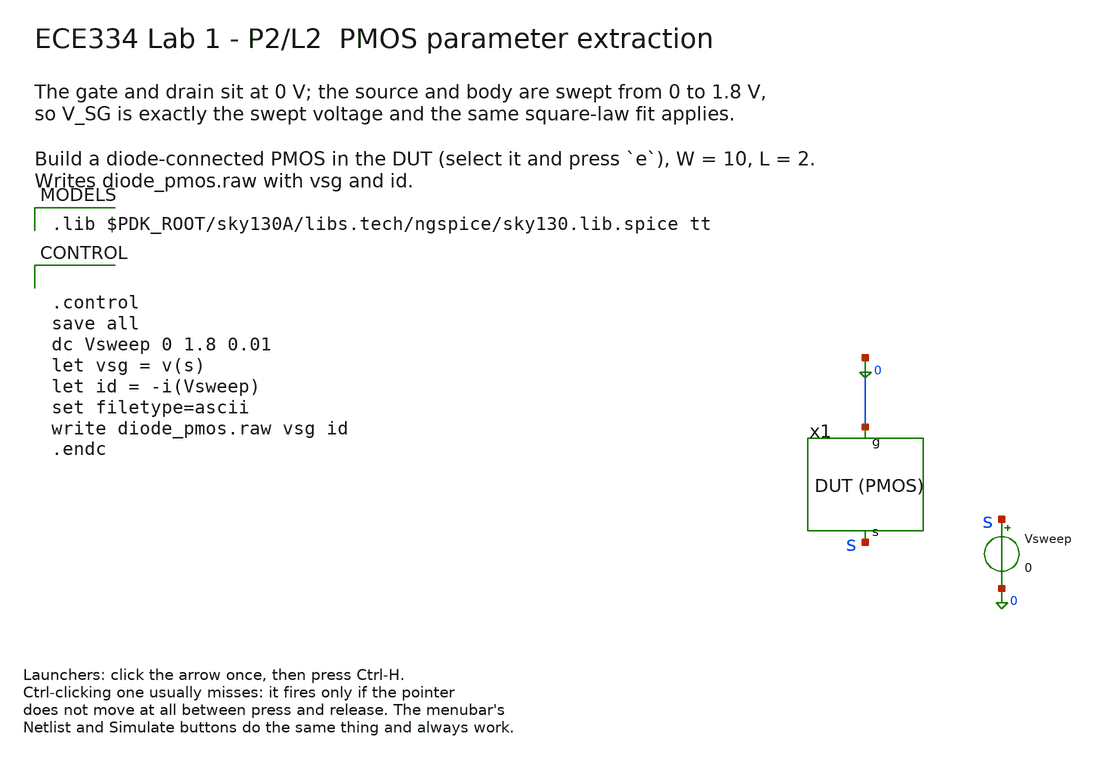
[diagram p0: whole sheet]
** sch_path: lab1_spice/xschem/diode_pmos_tb.sch
**.subckt diode_pmos_tb
x1 0 s dut_diodep
Vsweep s 0 0
**** begin user architecture code

.lib $PDK_ROOT/sky130A/libs.tech/ngspice/sky130.lib.spice tt



.control
save all
dc Vsweep 0 1.8 0.01
let vsg = v(s)
let id = -i(Vsweep)
set filetype=ascii
write diode_pmos.raw vsg id
.endc


**** end user architecture code
**.ends

* expanding   symbol:  dut_diodep.sym # of pins=2
** sym_path: lab1_spice/xschem/dut_diodep.sym
** sch_path: lab1_spice/xschem/dut_diodep.sch
.subckt dut_diodep g s
*.iopin g
*.iopin s
.ends

.end
